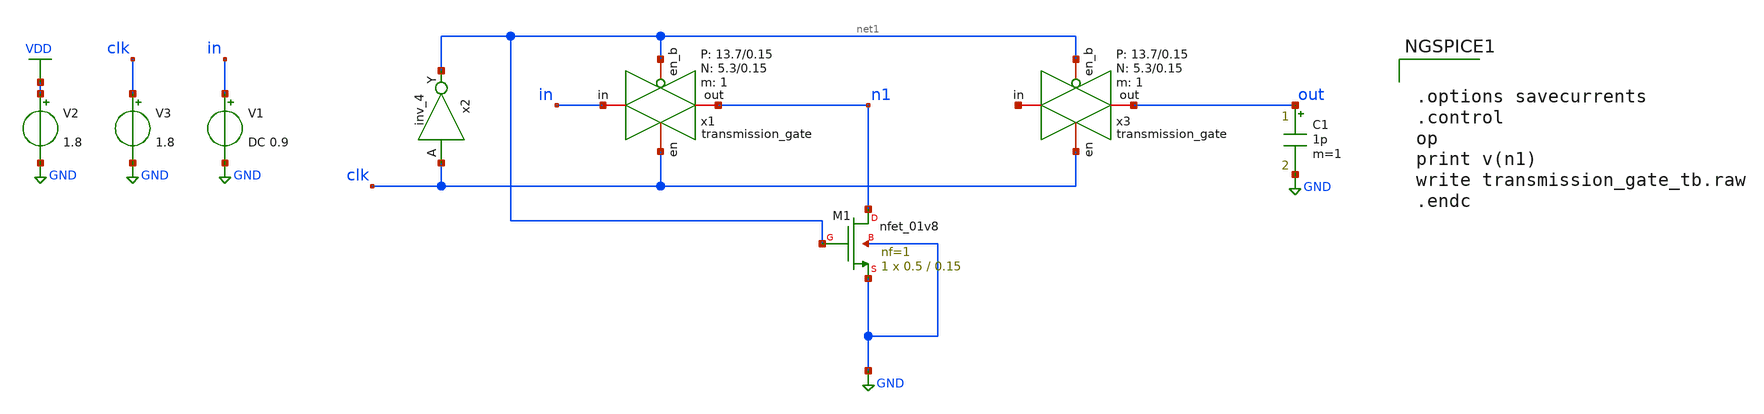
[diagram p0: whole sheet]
** sch_path: verification/schematic_sim/transmission_gate_tb.sch
**.subckt transmission_gate_tb
x2 clk GND GND VDD VDD net1 sky130_fd_sc_hd__inv_4
V2 VDD GND 1.8
V3 clk GND 1.8
V1 in GND DC 0.9
x1 in n1 clk net1 VDD VSS 1 5.3 0.15 13.7 0.15 transmission_gate
x3 net2 out clk net1 VDD VSS 1 5.3 0.15 13.7 0.15 transmission_gate
C1 out GND 1p m=1
XM1 n1 net1 GND GND sky130_fd_pr__nfet_01v8 L=0.15 W=0.5 nf=1 ad='int((nf+1)/2) * W/nf * 0.29' as='int((nf+2)/2) * W/nf * 0.29'
+ pd='2*int((nf+1)/2) * (W/nf + 0.29)' ps='2*int((nf+2)/2) * (W/nf + 0.29)' nrd='0.29 / W' nrs='0.29 / W'
+ sa=0 sb=0 sd=0 mult=1 m=1
**** begin user architecture code


.options savecurrents
.control
op
print v(n1)
write transmission_gate_tb.raw
.endc



** opencircuitdesign pdks install
.lib /farmshare/home/classes/ee/372/PDKs/open_pdks_1.0.310/sky130/sky130A/libs.tech/ngspice/sky130.lib.spice tt
.inc /farmshare/home/classes/ee/372/PDKs/open_pdks_1.0.310/sky130/sky130A/libs.ref/sky130_fd_sc_hd/spice/sky130_fd_sc_hd.spice

**** end user architecture code
**.ends

* expanding   symbol:  transmission_gate.sym # of pins=4
** sym_path: design/schematic/transmission_gate.sym
** sch_path: design/schematic/transmission_gate.sch
.subckt transmission_gate in out en en_b VDD VSS N W_N L_N W_P L_P    N=1 W_N=5.3 L_N=0.15 W_P=13.7
+ L_P=0.15
*.iopin in
*.iopin out
*.ipin en
*.ipin en_b
XM1 out en in VSS sky130_fd_pr__nfet_01v8 L=L_N W=W_N nf=1 ad='int((nf+1)/2) * W/nf * 0.29' as='int((nf+2)/2) * W/nf * 0.29'
+ pd='2*int((nf+1)/2) * (W/nf + 0.29)' ps='2*int((nf+2)/2) * (W/nf + 0.29)' nrd='0.29 / W' nrs='0.29 / W'
+ sa=0 sb=0 sd=0 mult=N m=N
XM2 out en_b in VDD sky130_fd_pr__pfet_01v8 L=L_P W=W_P nf=1 ad='int((nf+1)/2) * W/nf * 0.29' as='int((nf+2)/2) * W/nf * 0.29'
+ pd='2*int((nf+1)/2) * (W/nf + 0.29)' ps='2*int((nf+2)/2) * (W/nf + 0.29)' nrd='0.29 / W' nrs='0.29 / W'
+ sa=0 sb=0 sd=0 mult=N m=N
.ends

.GLOBAL GND
.GLOBAL VDD
.end
